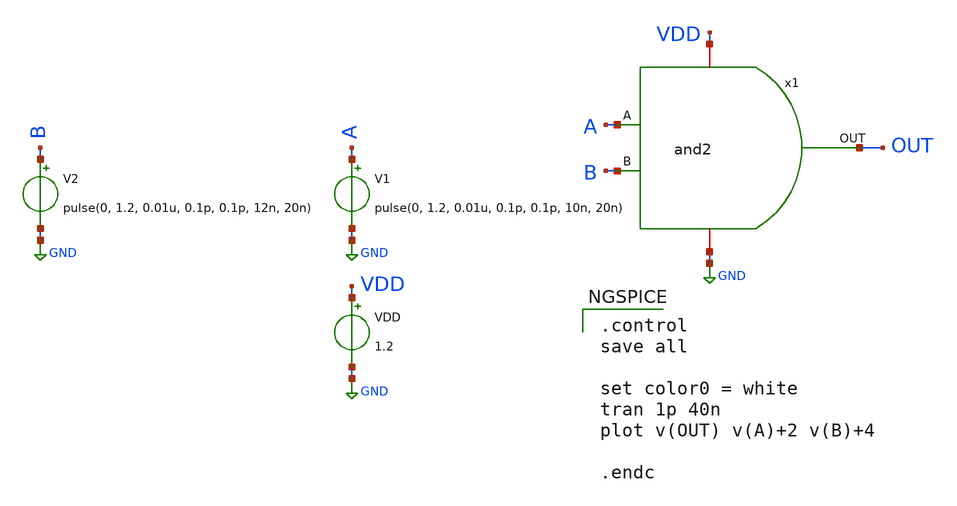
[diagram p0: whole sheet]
** sch_path: design/AND2/xschem/and2_tb.sch
**.subckt and2_tb
VDD VDD GND 1.2
V1 A GND pulse(0, 1.2, 0.01u, 0.1p, 0.1p, 10n, 20n)
x1 GND A B VDD OUT and2
V2 B GND pulse(0, 1.2, 0.01u, 0.1p, 0.1p, 12n, 20n)
**** begin user architecture code

** opencircuitdesign pdks install
.lib $::SKYWATER_MODELS/sky130.lib.spice tt_mm



.control
save all

set color0 = white
tran 1p 40n
plot v(OUT) v(A)+2 v(B)+4

.endc

**** end user architecture code
**.ends

* expanding   symbol:  and2.sym # of pins=5
** sym_path: design/CONTROL_UNIT/xschem/and2.sym
** sch_path: design/CONTROL_UNIT/xschem/and2.sch
.subckt and2 VSS A B VDD OUT
*.iopin VSS
*.ipin A
*.ipin B
*.iopin VDD
*.opin OUT
XM2 net2 B VSS VSS sky130_fd_pr__nfet_01v8 L=0.30 W=2 nf=2 ad='int((nf+1)/2) * W/nf * 0.29' as='int((nf+2)/2) * W/nf * 0.29'
+ pd='2*int((nf+1)/2) * (W/nf + 0.29)' ps='2*int((nf+2)/2) * (W/nf + 0.29)' nrd='0.29 / W' nrs='0.29 / W'
+ sa=0 sb=0 sd=0 mult=1 m=1
XM1 net1 A net2 VSS sky130_fd_pr__nfet_01v8 L=0.30 W=2 nf=2 ad='int((nf+1)/2) * W/nf * 0.29' as='int((nf+2)/2) * W/nf * 0.29'
+ pd='2*int((nf+1)/2) * (W/nf + 0.29)' ps='2*int((nf+2)/2) * (W/nf + 0.29)' nrd='0.29 / W' nrs='0.29 / W'
+ sa=0 sb=0 sd=0 mult=1 m=1
XM3 net1 A VDD VDD sky130_fd_pr__pfet_01v8 L=0.3 W=3 nf=3 ad='int((nf+1)/2) * W/nf * 0.29' as='int((nf+2)/2) * W/nf * 0.29'
+ pd='2*int((nf+1)/2) * (W/nf + 0.29)' ps='2*int((nf+2)/2) * (W/nf + 0.29)' nrd='0.29 / W' nrs='0.29 / W'
+ sa=0 sb=0 sd=0 mult=1 m=1
XM4 net1 B VDD VDD sky130_fd_pr__pfet_01v8 L=0.30 W=3 nf=3 ad='int((nf+1)/2) * W/nf * 0.29' as='int((nf+2)/2) * W/nf * 0.29'
+ pd='2*int((nf+1)/2) * (W/nf + 0.29)' ps='2*int((nf+2)/2) * (W/nf + 0.29)' nrd='0.29 / W' nrs='0.29 / W'
+ sa=0 sb=0 sd=0 mult=1 m=1
XM5 OUT net1 VDD VDD sky130_fd_pr__pfet_01v8 L=0.30 W=3 nf=3 ad='int((nf+1)/2) * W/nf * 0.29' as='int((nf+2)/2) * W/nf * 0.29'
+ pd='2*int((nf+1)/2) * (W/nf + 0.29)' ps='2*int((nf+2)/2) * (W/nf + 0.29)' nrd='0.29 / W' nrs='0.29 / W'
+ sa=0 sb=0 sd=0 mult=1 m=1
XM6 OUT net1 VSS VSS sky130_fd_pr__nfet_01v8 L=0.30 W=2 nf=2 ad='int((nf+1)/2) * W/nf * 0.29' as='int((nf+2)/2) * W/nf * 0.29'
+ pd='2*int((nf+1)/2) * (W/nf + 0.29)' ps='2*int((nf+2)/2) * (W/nf + 0.29)' nrd='0.29 / W' nrs='0.29 / W'
+ sa=0 sb=0 sd=0 mult=1 m=1
.ends

.GLOBAL GND
.end
